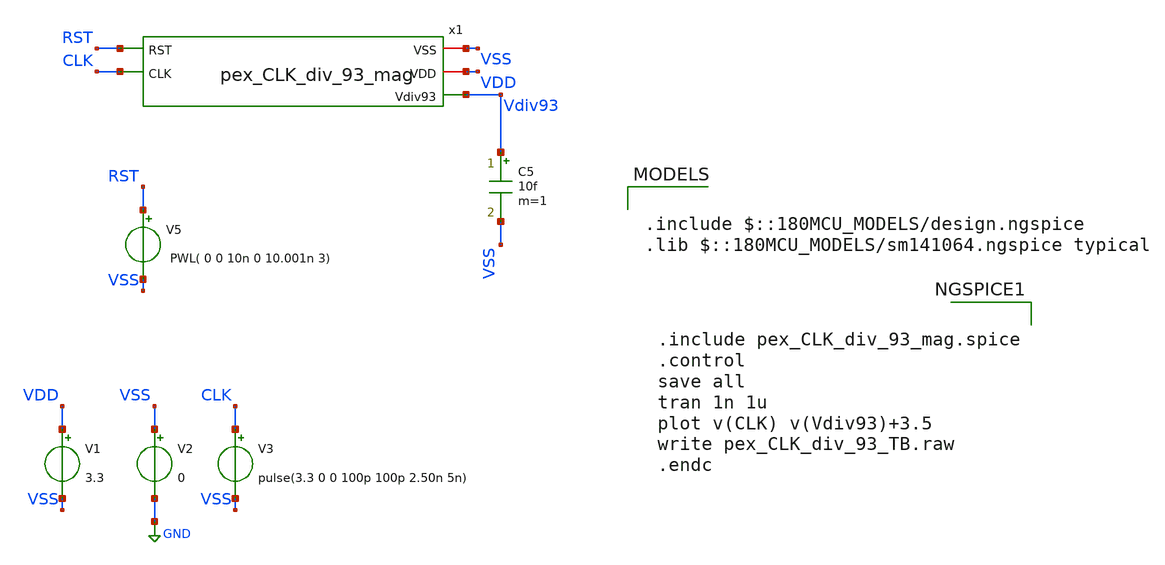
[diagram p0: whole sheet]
** sch_path: Clock_Generator_PAKISTAN_02/Schematics/pex_CLK_div_93_mag_tb.sch
**.subckt pex_CLK_div_93_mag_tb
V1 VDD VSS 3.3
V2 VSS GND 0
V3 CLK VSS pulse(3.3 0 0 100p 100p 2.50n 5n)
C5 Vdiv93 VSS 10f m=1
V5 RST VSS PWL( 0 0 10n 0 10.001n 3)
x1 VSS VDD Vdiv93 RST CLK pex_CLK_div_93_mag
**** begin user architecture code

.include $::180MCU_MODELS/design.ngspice
.lib $::180MCU_MODELS/sm141064.ngspice typical



.include pex_CLK_div_93_mag.spice
.control
save all
tran 1n 1u
plot v(CLK) v(Vdiv93)+3.5
write pex_CLK_div_93_TB.raw
.endc


**** end user architecture code
**.ends
.GLOBAL GND
.end
